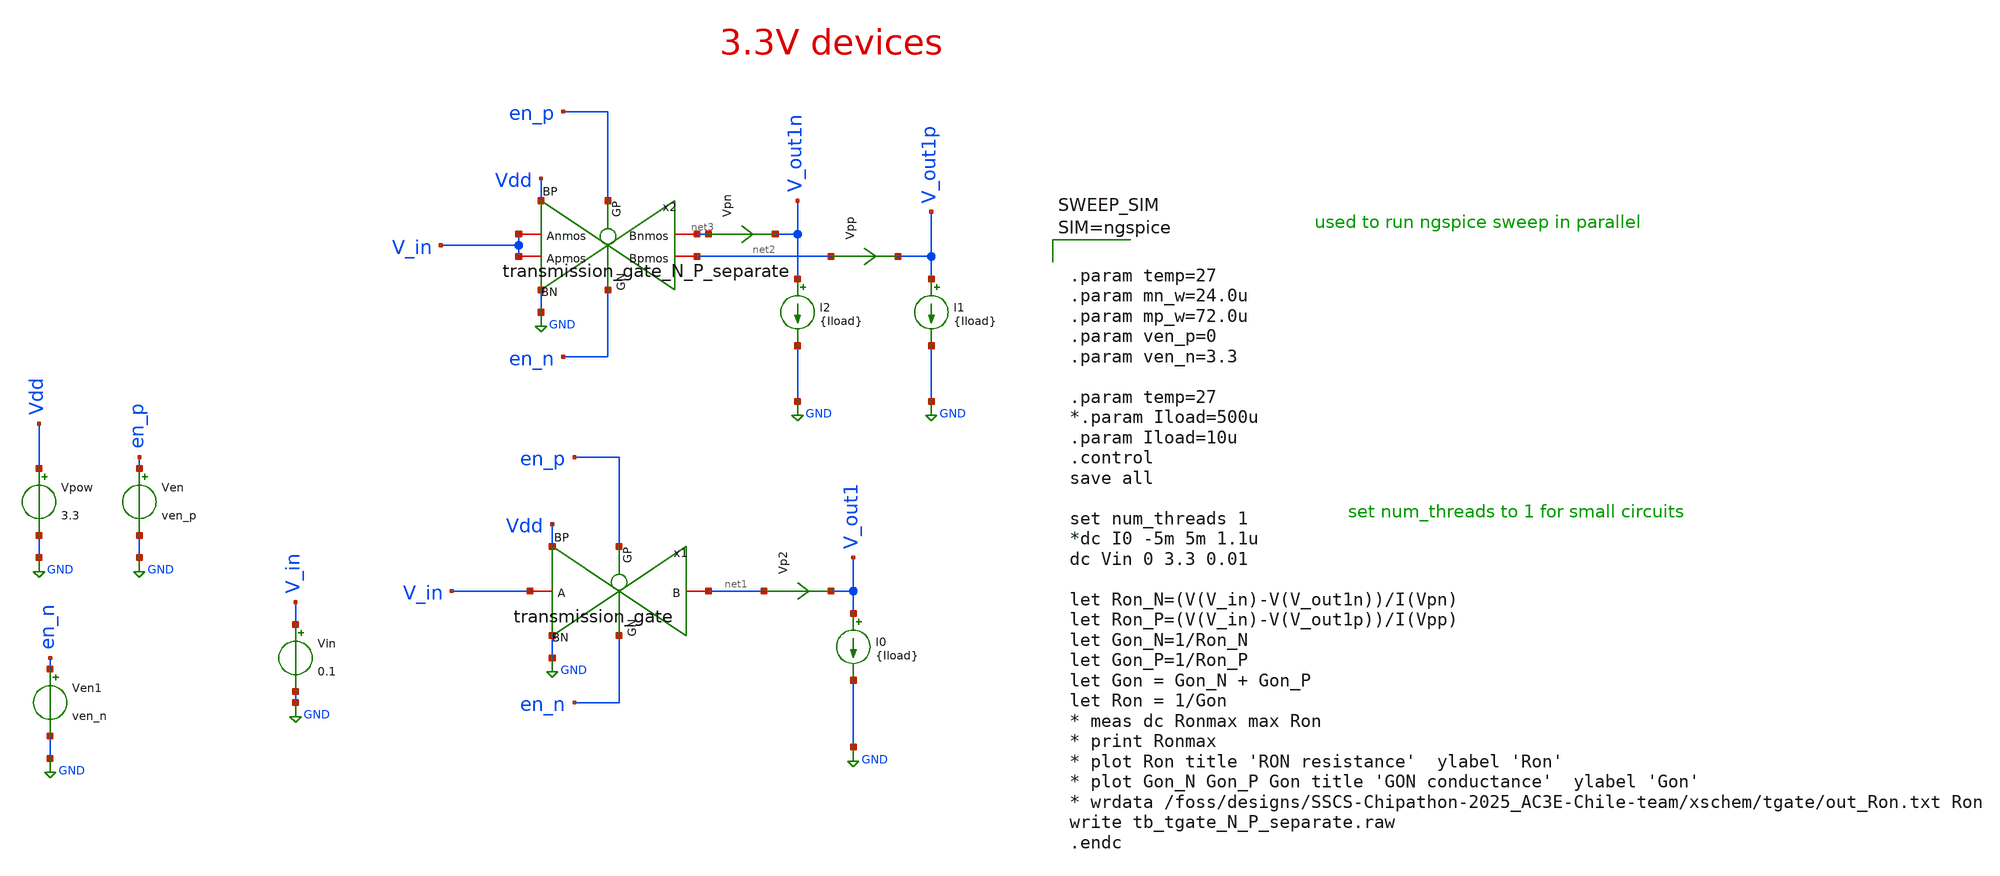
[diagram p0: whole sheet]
** sch_path: designs/switch_matrix_gf180mcu_9t5v0-main/tgate_PK/tgate_N_P_separate_lv_vsweep_tb.sch
**.subckt tgate_N_P_separate_lv_vsweep_tb
Vpow Vdd GND 3.3
Vin V_in GND 0.1
Ven en_p GND ven_p
Ven1 en_n GND ven_n
I0 V_out1 GND {Iload}
Vp2 net1 V_out1 0
.save i(vp2)
x1 net1 en_n en_p V_in Vdd GND transmission_gate
I1 V_out1p GND {Iload}
Vpp net2 V_out1p 0
.save i(vpp)
x2 net3 en_n en_p V_in Vdd GND net2 V_in transmission_gate_N_P_separate
I2 V_out1n GND {Iload}
Vpn net3 V_out1n 0
.save i(vpn)
**** begin user architecture code



.param temp=27
.param mn_w=24.0u
.param mp_w=72.0u
.param ven_p=0
.param ven_n=3.3

.param temp=27
*.param Iload=500u
.param Iload=10u
.control
save all

set num_threads 1
*dc I0 -5m 5m 1.1u
dc Vin 0 3.3 0.01

let Ron_N=(V(V_in)-V(V_out1n))/I(Vpn)
let Ron_P=(V(V_in)-V(V_out1p))/I(Vpp)
let Gon_N=1/Ron_N
let Gon_P=1/Ron_P
let Gon = Gon_N + Gon_P
let Ron = 1/Gon
* meas dc Ronmax max Ron
* print Ronmax
* plot Ron title 'RON resistance'  ylabel 'Ron'
* plot Gon_N Gon_P Gon title 'GON conductance'  ylabel 'Gon'
* wrdata /foss/designs/SSCS-Chipathon-2025_AC3E-Chile-team/xschem/tgate/out_Ron.txt Ron
write tb_tgate_N_P_separate.raw
.endc




.include $::180MCU_MODELS/design.ngspice
.lib $::180MCU_MODELS/sm141064.ngspice typical

.include /foss/pdks/gf180mcuD/libs.ref/gf180mcu_fd_sc_mcu7t5v0/spice/gf180mcu_fd_sc_mcu7t5v0.spice

**** end user architecture code
**.ends
.GLOBAL GND
.end
